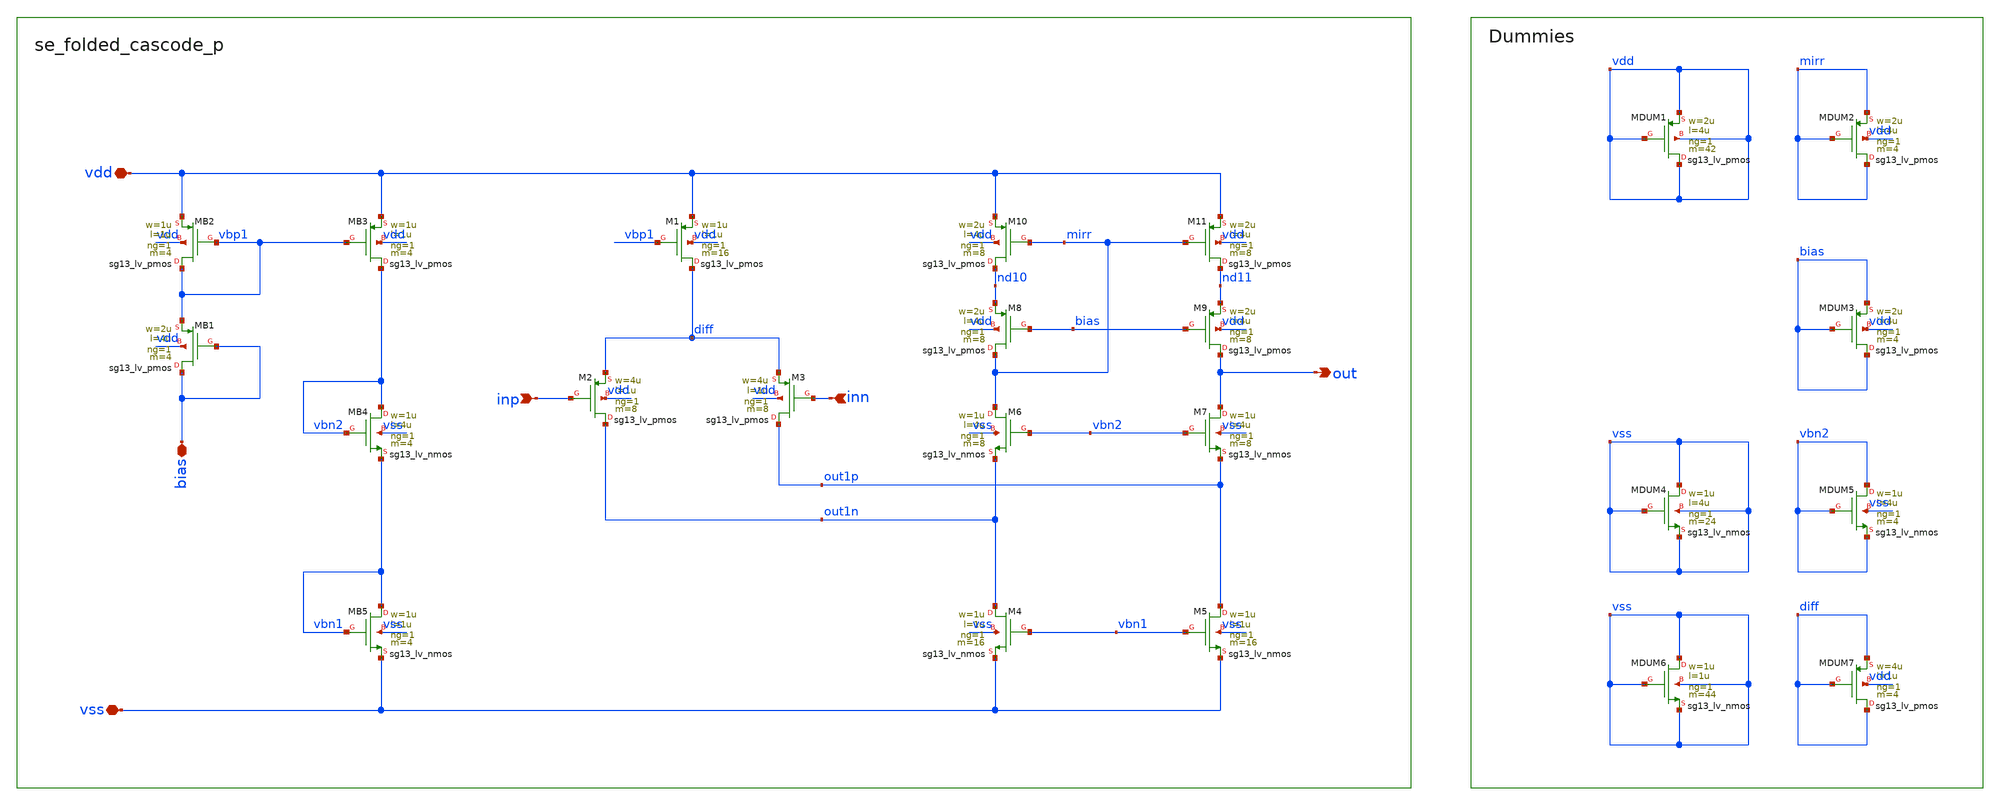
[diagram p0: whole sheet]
** sch_path: xschem/bandgap_orig/se_folded_cascode_p.sch
**.subckt se_folded_cascode_p inn inp out bias vdd vss
*.ipin inn
*.ipin inp
*.opin out
*.iopin bias
*.iopin vdd
*.iopin vss
XM3 out1p inn diff vdd sg13_lv_pmos w=4u l=1u ng=1 m=8 mm_ok=1
XM2 out1n inp diff vdd sg13_lv_pmos w=4u l=1u ng=1 m=8 mm_ok=1
XM1 diff vbp1 vdd vdd sg13_lv_pmos w=1u l=1u ng=1 m=16 mm_ok=1
XM4 out1n vbn1 vss vss sg13_lv_nmos w=1u l=1u ng=1 m=16 mm_ok=1
XM5 out1p vbn1 vss vss sg13_lv_nmos w=1u l=1u ng=1 m=16 mm_ok=1
XM6 mirr vbn2 out1n vss sg13_lv_nmos w=1u l=4u ng=1 m=8 mm_ok=1
XM7 out vbn2 out1p vss sg13_lv_nmos w=1u l=4u ng=1 m=8 mm_ok=1
XM8 mirr bias nd10 vdd sg13_lv_pmos w=2u l=4u ng=1 m=8 mm_ok=1
XM9 out bias nd11 vdd sg13_lv_pmos w=2u l=4u ng=1 m=8 mm_ok=1
XM10 nd10 mirr vdd vdd sg13_lv_pmos w=2u l=4u ng=1 m=8 mm_ok=1
XM11 nd11 mirr vdd vdd sg13_lv_pmos w=2u l=4u ng=1 m=8 mm_ok=1
XMB1 bias bias vbp1 vdd sg13_lv_pmos w=2u l=4u ng=1 m=4 mm_ok=1
XMB2 vbp1 vbp1 vdd vdd sg13_lv_pmos w=1u l=1u ng=1 m=4 mm_ok=1
XMB3 vbn2 vbp1 vdd vdd sg13_lv_pmos w=1u l=1u ng=1 m=4 mm_ok=1
XMB4 vbn2 vbn2 vbn1 vss sg13_lv_nmos w=1u l=4u ng=1 m=4 mm_ok=1
XMB5 vbn1 vbn1 vss vss sg13_lv_nmos w=1u l=1u ng=1 m=4 mm_ok=1
XMDUM1 vdd vdd vdd vdd sg13_lv_pmos w=2u l=4u ng=1 m=42 mm_ok=1
XMDUM2 mirr mirr mirr vdd sg13_lv_pmos w=2u l=4u ng=1 m=4 mm_ok=1
XMDUM3 bias bias bias vdd sg13_lv_pmos w=2u l=4u ng=1 m=4 mm_ok=1
XMDUM4 vss vss vss vss sg13_lv_nmos w=1u l=4u ng=1 m=24 mm_ok=1
XMDUM5 vbn2 vbn2 vbn2 vss sg13_lv_nmos w=1u l=4u ng=1 m=4 mm_ok=1
XMDUM6 vss vss vss vss sg13_lv_nmos w=1u l=1u ng=1 m=44 mm_ok=1
XMDUM7 diff diff diff vdd sg13_lv_pmos w=4u l=1u ng=1 m=4 mm_ok=1
**.ends
.end
